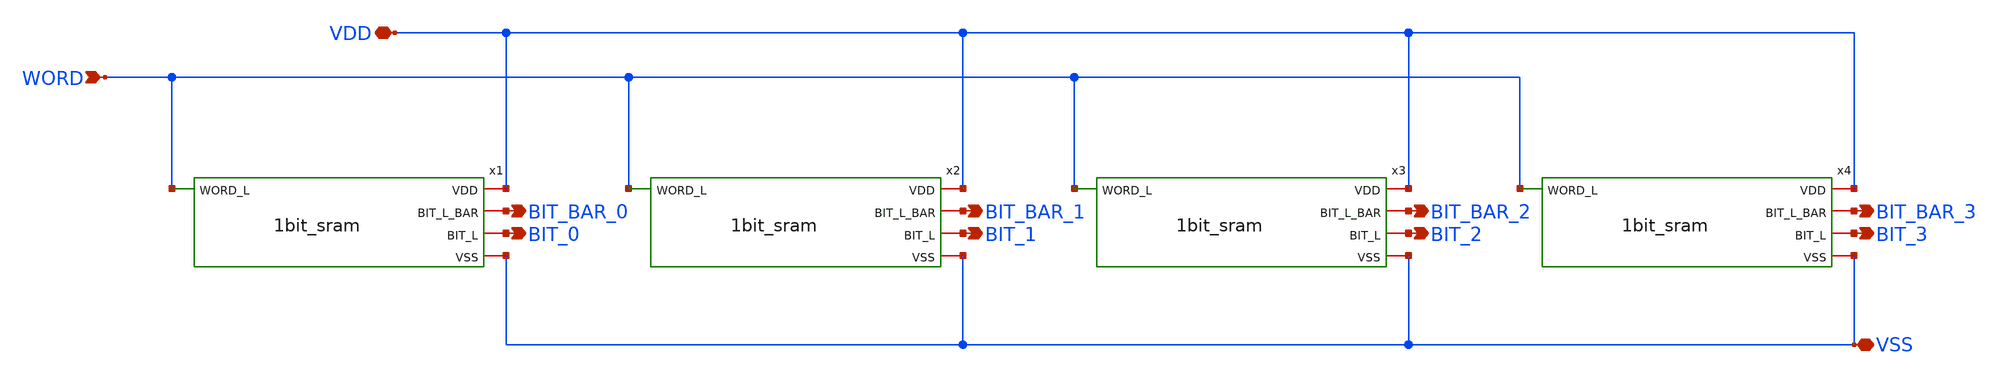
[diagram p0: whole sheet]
** sch_path: member_project/SRAM/noritsuna/4bit_sram.sch
**.subckt 4bit_sram VDD BIT_BAR_0 BIT_BAR_1 BIT_BAR_2 BIT_BAR_3 BIT_0 BIT_1 BIT_2 BIT_3 WORD VSS
*.iopin VDD
*.opin BIT_BAR_0
*.opin BIT_BAR_1
*.opin BIT_BAR_2
*.opin BIT_BAR_3
*.opin BIT_0
*.opin BIT_1
*.opin BIT_2
*.opin BIT_3
*.ipin WORD
*.iopin VSS
x1 WORD VDD BIT_BAR_0 BIT_0 VSS 1bit_sram
x2 WORD VDD BIT_BAR_1 BIT_1 VSS 1bit_sram
x3 WORD VDD BIT_BAR_2 BIT_2 VSS 1bit_sram
x4 WORD VDD BIT_BAR_3 BIT_3 VSS 1bit_sram
**.ends

* expanding   symbol:  1bit_sram.sym # of pins=5
** sym_path: member_project/SRAM/noritsuna/1bit_sram.sym
** sch_path: member_project/SRAM/noritsuna/1bit_sram.sch
.subckt 1bit_sram WORD_L VDD BIT_L_BAR BIT_L VSS
*.iopin VDD
*.iopin VSS
*.iopin BIT_L_BAR
*.iopin BIT_L
*.ipin WORD_L
XXM1 net2 net1 VDD VDD PMOS w=24u l=4.2u nrd=0 nrs=0 m=12
XXM2 net2 net1 VSS VSS NMOS w=24u l=4.2u nrd=0 nrs=0 m=40
XXM3 net1 net2 VDD VDD PMOS w=24u l=4.2u nrd=0 nrs=0 m=12
XXM4 net1 net2 VSS VSS NMOS w=24u l=4.2u nrd=0 nrs=0 m=40
XXM5 BIT_L_BAR WORD_L net1 VSS NMOS w=24u l=4.2u nrd=0 nrs=0 m=20
XXM6 BIT_L WORD_L net2 VSS NMOS w=24u l=4.2u nrd=0 nrs=0 m=20
.ends

.end
